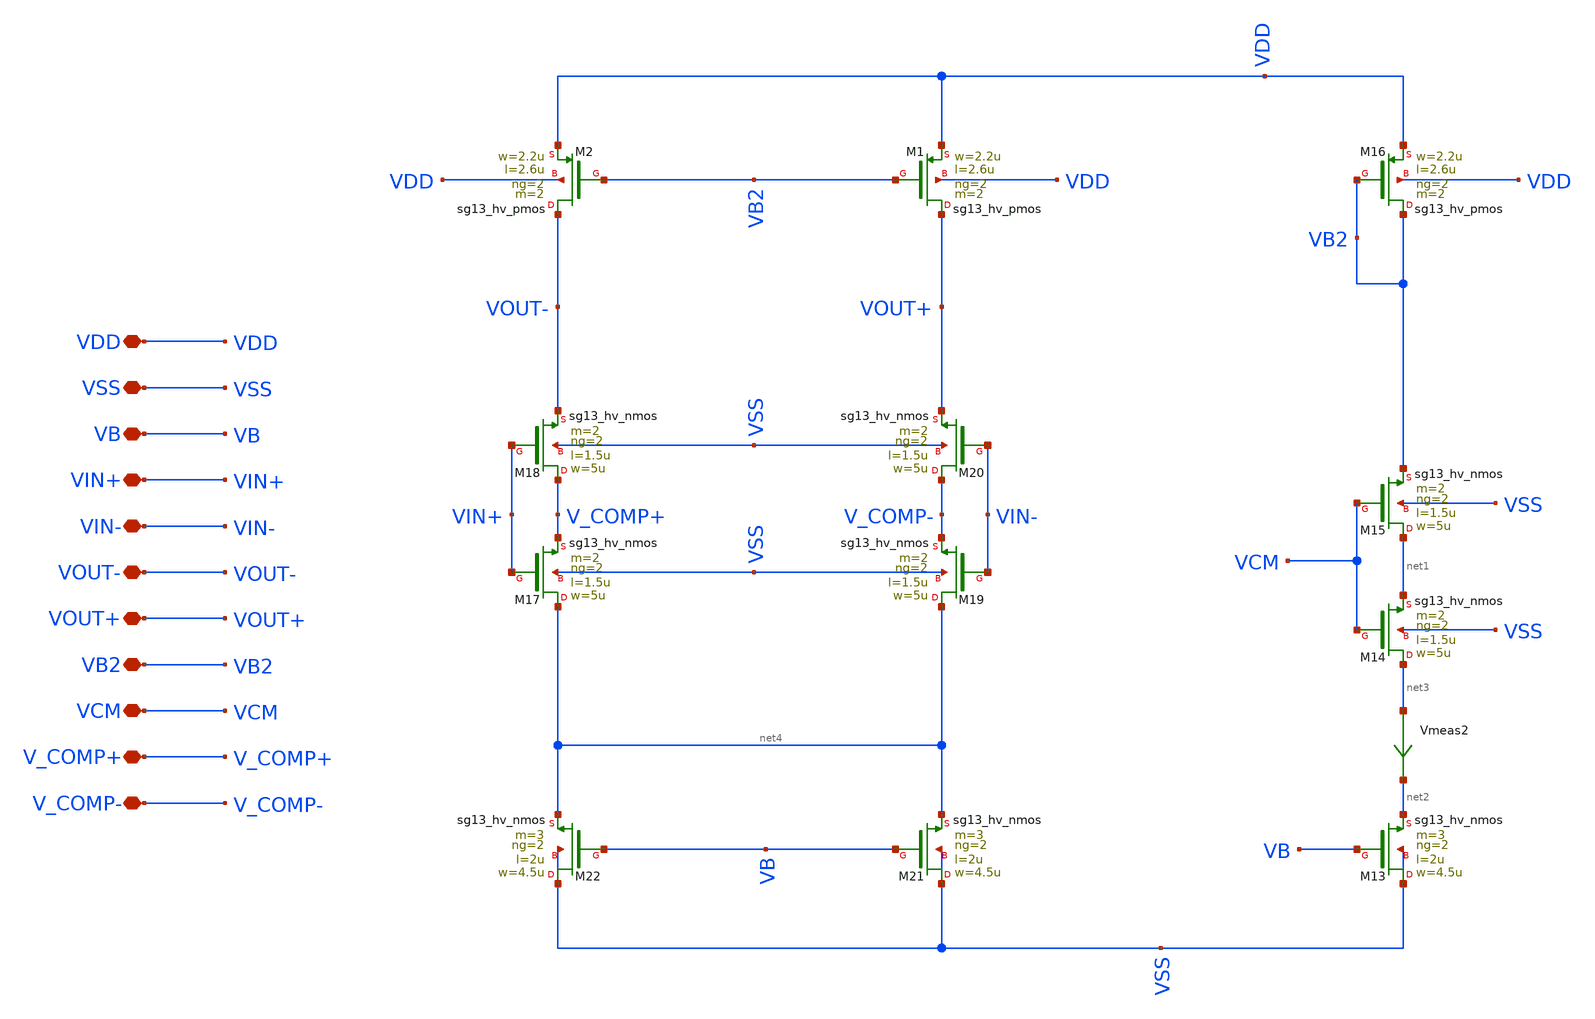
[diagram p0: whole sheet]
** sch_path: LIB/ihp-sg13g2/FD_opamp001/first_stage.sch
**.subckt first_stage VDD VSS VB VIN+ VIN- VOUT- VOUT+ VB2 VCM V_COMP+ V_COMP-
*.iopin VDD
*.iopin VSS
*.iopin VB
*.iopin VIN+
*.iopin VIN-
*.iopin VOUT-
*.iopin VOUT+
*.iopin VB2
*.iopin VCM
*.iopin V_COMP+
*.iopin V_COMP-
XM13 VSS VB net2 VSS sg13_hv_nmos w=4.5u l=2u ng=2 m=3 mm_ok=1
XM14 net3 VCM net1 VSS sg13_hv_nmos w=5u l=1.5u ng=2 m=2 mm_ok=1
XM15 net1 VCM VB2 VSS sg13_hv_nmos w=5u l=1.5u ng=2 m=2 mm_ok=1
XM16 VB2 VB2 VDD VDD sg13_hv_pmos w=2.2u l=2.6u ng=2 m=2 mm_ok=1
Vmeas2 net3 net2 0
.save i(vmeas2)
XM17 net4 VIN+ V_COMP+ VSS sg13_hv_nmos w=5u l=1.5u ng=2 m=2 mm_ok=1
XM18 V_COMP+ VIN+ VOUT- VSS sg13_hv_nmos w=5u l=1.5u ng=2 m=2 mm_ok=1
XM19 net4 VIN- V_COMP- VSS sg13_hv_nmos w=5u l=1.5u ng=2 m=2 mm_ok=1
XM20 V_COMP- VIN- VOUT+ VSS sg13_hv_nmos w=5u l=1.5u ng=2 m=2 mm_ok=1
XM21 VSS VB net4 VSS sg13_hv_nmos w=4.5u l=2u ng=2 m=3 mm_ok=1
XM22 VSS VB net4 VSS sg13_hv_nmos w=4.5u l=2u ng=2 m=3 mm_ok=1
XM1 VOUT+ VB2 VDD VDD sg13_hv_pmos w=2.2u l=2.6u ng=2 m=2 mm_ok=1
XM2 VOUT- VB2 VDD VDD sg13_hv_pmos w=2.2u l=2.6u ng=2 m=2 mm_ok=1
**.ends
.end
